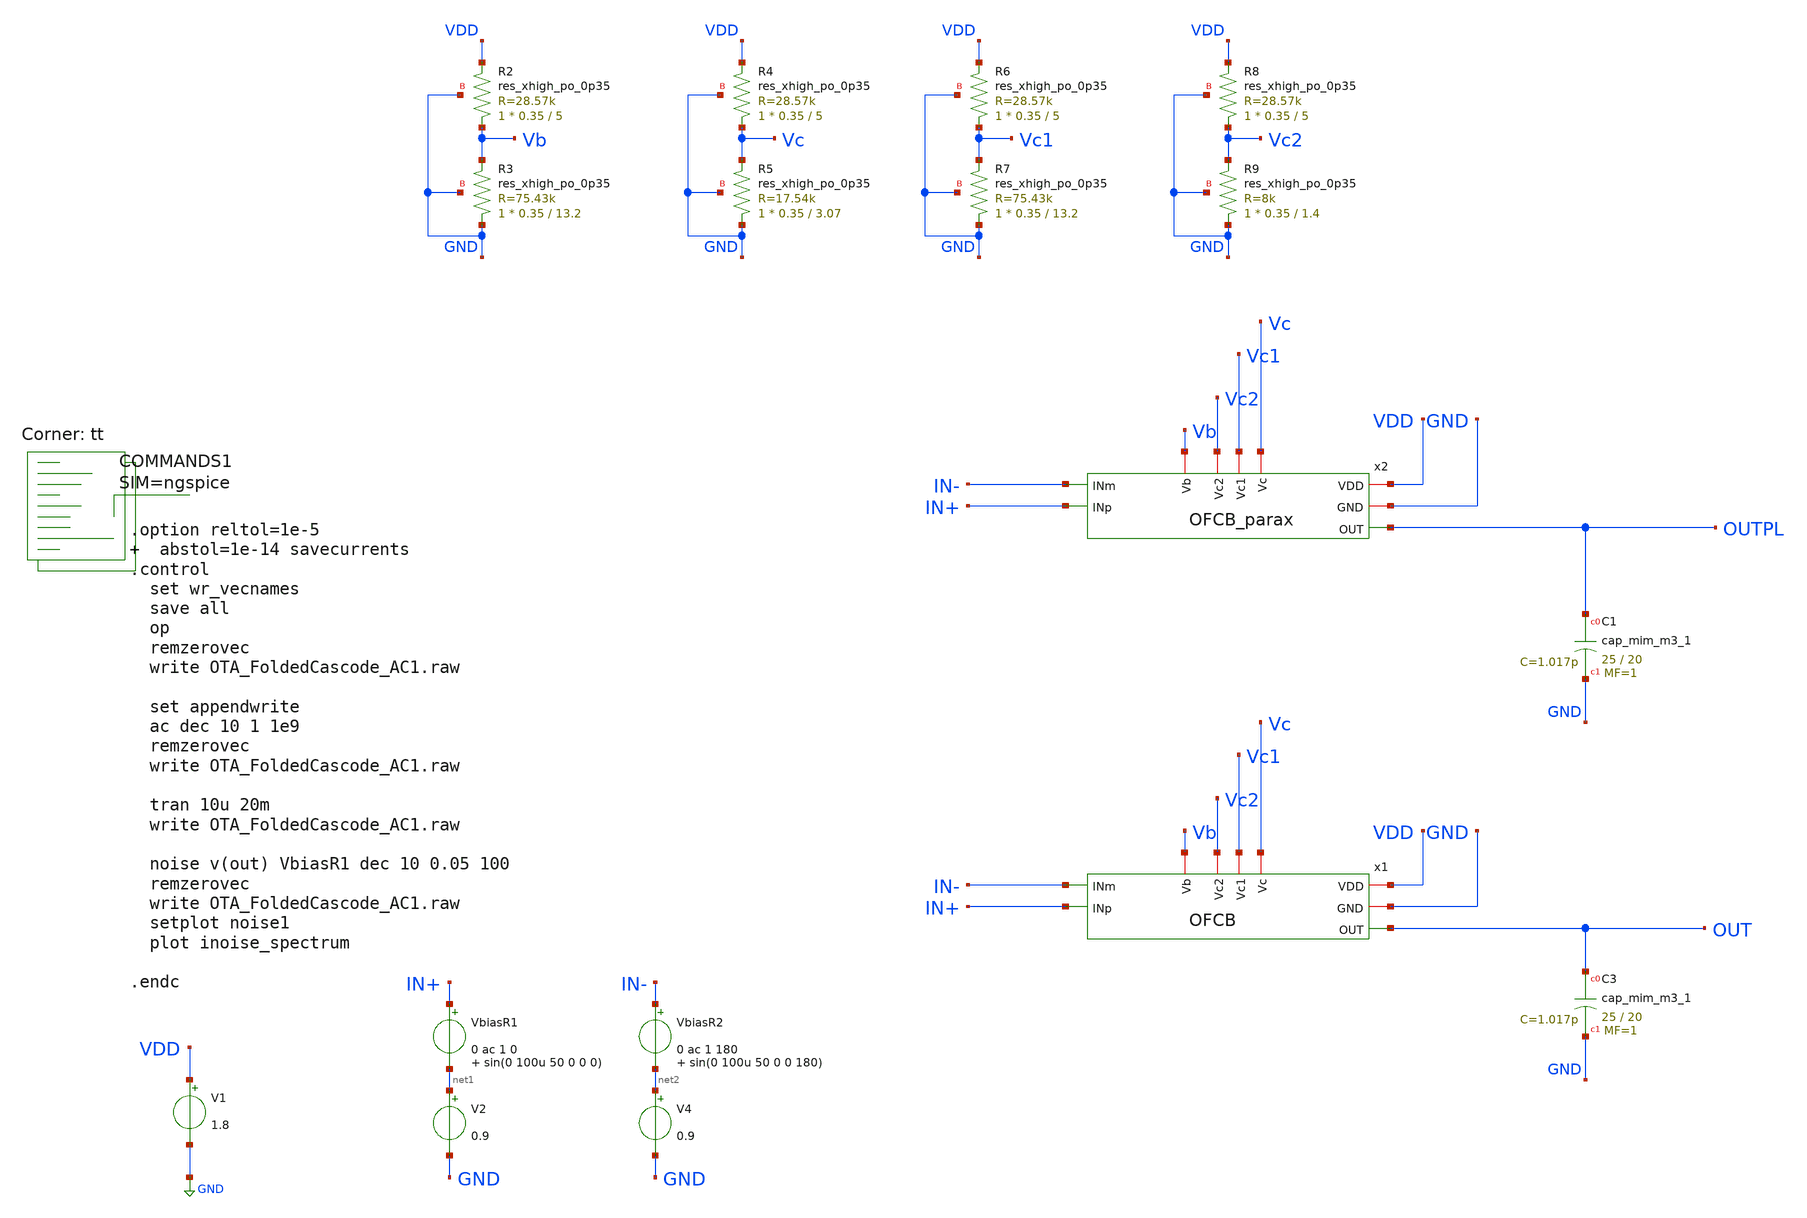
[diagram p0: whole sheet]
** sch_path: xschem/OTA_FoldedCascode_AC1.sch
**.subckt OTA_FoldedCascode_AC1
VbiasR1 IN+ net1 0 ac 1 0 sin(0 100u 50 0 0 0)
V2 net1 GND 0.9
XC3 OUT GND sky130_fd_pr__cap_mim_m3_1 W=25 L=20 MF=1 m=1
V1 VDD GND 1.8
XC1 OUTPL GND sky130_fd_pr__cap_mim_m3_1 W=25 L=20 MF=1 m=1
x1 Vb VDD GND Vc2 OUT IN+ IN- Vc1 Vc OFCB
x2 Vb VDD GND Vc2 OUTPL IN+ IN- Vc1 Vc OFCB_parax
VbiasR2 IN- net2 0 ac 1 180 sin(0 100u 50 0 0 180)
V4 net2 GND 0.9
XR2 Vb VDD GND sky130_fd_pr__res_xhigh_po_0p35 L=5 mult=1 m=1
XR3 GND Vb GND sky130_fd_pr__res_xhigh_po_0p35 L=13.2 mult=1 m=1
XR4 Vc VDD GND sky130_fd_pr__res_xhigh_po_0p35 L=5 mult=1 m=1
XR5 GND Vc GND sky130_fd_pr__res_xhigh_po_0p35 L=3.07 mult=1 m=1
XR6 Vc1 VDD GND sky130_fd_pr__res_xhigh_po_0p35 L=5 mult=1 m=1
XR7 GND Vc1 GND sky130_fd_pr__res_xhigh_po_0p35 L=13.2 mult=1 m=1
XR8 Vc2 VDD GND sky130_fd_pr__res_xhigh_po_0p35 L=5 mult=1 m=1
XR9 GND Vc2 GND sky130_fd_pr__res_xhigh_po_0p35 L=1.4 mult=1 m=1
**** begin user architecture code



.option reltol=1e-5   abstol=1e-14 savecurrents
.control
  set wr_vecnames
  save all
  op
  remzerovec
  write OTA_FoldedCascode_AC1.raw

  set appendwrite
  ac dec 10 1 1e9
  remzerovec
  write OTA_FoldedCascode_AC1.raw

  tran 10u 20m
  write OTA_FoldedCascode_AC1.raw

  noise v(out) VbiasR1 dec 10 0.05 100
  remzerovec
  write OTA_FoldedCascode_AC1.raw
  setplot noise1
  plot inoise_spectrum

.endc



.lib $::SKYWATER_MODELS/sky130.lib.spice tt
**** end user architecture code
**.ends

* expanding   symbol:  OFCB.sym # of pins=9
** sym_path: xschem/OFCB.sym
** sch_path: xschem/OFCB.sch
.subckt OFCB Vb VDD GND Vc2 OUT INp INm Vc1 Vc
*.iopin VDD
*.iopin GND
*.opin OUT
*.ipin INp
*.ipin INm
*.iopin Vc2
*.iopin Vc1
*.iopin Vc
*.iopin Vb
XM11 S Vb VDD VDD sky130_fd_pr__pfet_01v8_lvt L=1 W=60 nf=6 ad='int((nf+1)/2) * W/nf * 0.29' as='int((nf+2)/2) * W/nf * 0.29'
+ pd='2*int((nf+1)/2) * (W/nf + 0.29)' ps='2*int((nf+2)/2) * (W/nf + 0.29)' nrd='0.29 / W' nrs='0.29 / W'
+ sa=0 sb=0 sd=0 mult=2 m=2
XM1 D1 INp S S sky130_fd_pr__pfet_01v8_lvt L=10 W=25 nf=2 ad='int((nf+1)/2) * W/nf * 0.29' as='int((nf+2)/2) * W/nf * 0.29'
+ pd='2*int((nf+1)/2) * (W/nf + 0.29)' ps='2*int((nf+2)/2) * (W/nf + 0.29)' nrd='0.29 / W' nrs='0.29 / W'
+ sa=0 sb=0 sd=0 mult=2 m=2
XM2 D2 INm S S sky130_fd_pr__pfet_01v8_lvt L=10 W=25 nf=2 ad='int((nf+1)/2) * W/nf * 0.29' as='int((nf+2)/2) * W/nf * 0.29'
+ pd='2*int((nf+1)/2) * (W/nf + 0.29)' ps='2*int((nf+2)/2) * (W/nf + 0.29)' nrd='0.29 / W' nrs='0.29 / W'
+ sa=0 sb=0 sd=0 mult=2 m=2
XM3 OUT Vc1 D2 GND sky130_fd_pr__nfet_01v8_lvt L=1 W=4 nf=1 ad='int((nf+1)/2) * W/nf * 0.29' as='int((nf+2)/2) * W/nf * 0.29'
+ pd='2*int((nf+1)/2) * (W/nf + 0.29)' ps='2*int((nf+2)/2) * (W/nf + 0.29)' nrd='0.29 / W' nrs='0.29 / W'
+ sa=0 sb=0 sd=0 mult=1 m=1
XM4 D2 Vc GND GND sky130_fd_pr__nfet_01v8_lvt L=1 W=2.8 nf=1 ad='int((nf+1)/2) * W/nf * 0.29' as='int((nf+2)/2) * W/nf * 0.29'
+ pd='2*int((nf+1)/2) * (W/nf + 0.29)' ps='2*int((nf+2)/2) * (W/nf + 0.29)' nrd='0.29 / W' nrs='0.29 / W'
+ sa=0 sb=0 sd=0 mult=1 m=1
XM5 D1 Vc GND GND sky130_fd_pr__nfet_01v8_lvt L=1 W=2.8 nf=1 ad='int((nf+1)/2) * W/nf * 0.29' as='int((nf+2)/2) * W/nf * 0.29'
+ pd='2*int((nf+1)/2) * (W/nf + 0.29)' ps='2*int((nf+2)/2) * (W/nf + 0.29)' nrd='0.29 / W' nrs='0.29 / W'
+ sa=0 sb=0 sd=0 mult=1 m=1
XM6 G Vc1 D1 GND sky130_fd_pr__nfet_01v8_lvt L=1 W=4 nf=1 ad='int((nf+1)/2) * W/nf * 0.29' as='int((nf+2)/2) * W/nf * 0.29'
+ pd='2*int((nf+1)/2) * (W/nf + 0.29)' ps='2*int((nf+2)/2) * (W/nf + 0.29)' nrd='0.29 / W' nrs='0.29 / W'
+ sa=0 sb=0 sd=0 mult=1 m=1
XM7 G Vc2 D9 D9 sky130_fd_pr__pfet_01v8_lvt L=2.23 W=4 nf=1 ad='int((nf+1)/2) * W/nf * 0.29' as='int((nf+2)/2) * W/nf * 0.29'
+ pd='2*int((nf+1)/2) * (W/nf + 0.29)' ps='2*int((nf+2)/2) * (W/nf + 0.29)' nrd='0.29 / W' nrs='0.29 / W'
+ sa=0 sb=0 sd=0 mult=1 m=1
XM9 D9 G VDD VDD sky130_fd_pr__pfet_01v8_lvt L=2.23 W=3.85 nf=1 ad='int((nf+1)/2) * W/nf * 0.29' as='int((nf+2)/2) * W/nf * 0.29'
+ pd='2*int((nf+1)/2) * (W/nf + 0.29)' ps='2*int((nf+2)/2) * (W/nf + 0.29)' nrd='0.29 / W' nrs='0.29 / W'
+ sa=0 sb=0 sd=0 mult=1 m=1
XM8 D10 G VDD VDD sky130_fd_pr__pfet_01v8_lvt L=2.23 W=3.85 nf=1 ad='int((nf+1)/2) * W/nf * 0.29' as='int((nf+2)/2) * W/nf * 0.29'
+ pd='2*int((nf+1)/2) * (W/nf + 0.29)' ps='2*int((nf+2)/2) * (W/nf + 0.29)' nrd='0.29 / W' nrs='0.29 / W'
+ sa=0 sb=0 sd=0 mult=1 m=1
XM10 OUT Vc2 D10 D10 sky130_fd_pr__pfet_01v8_lvt L=2.23 W=4 nf=1 ad='int((nf+1)/2) * W/nf * 0.29' as='int((nf+2)/2) * W/nf * 0.29'
+ pd='2*int((nf+1)/2) * (W/nf + 0.29)' ps='2*int((nf+2)/2) * (W/nf + 0.29)' nrd='0.29 / W' nrs='0.29 / W'
+ sa=0 sb=0 sd=0 mult=1 m=1
XC1 OUT D1 sky130_fd_pr__cap_mim_m3_1 W=22.4 L=22.4 MF=2 m=2
.ends


* expanding   symbol:  OFCB_parax.sym # of pins=9
** sym_path: xschem/OFCB.sym
.include [file normalize ../mag/OFCB.sim.spice]
.GLOBAL GND
.end
